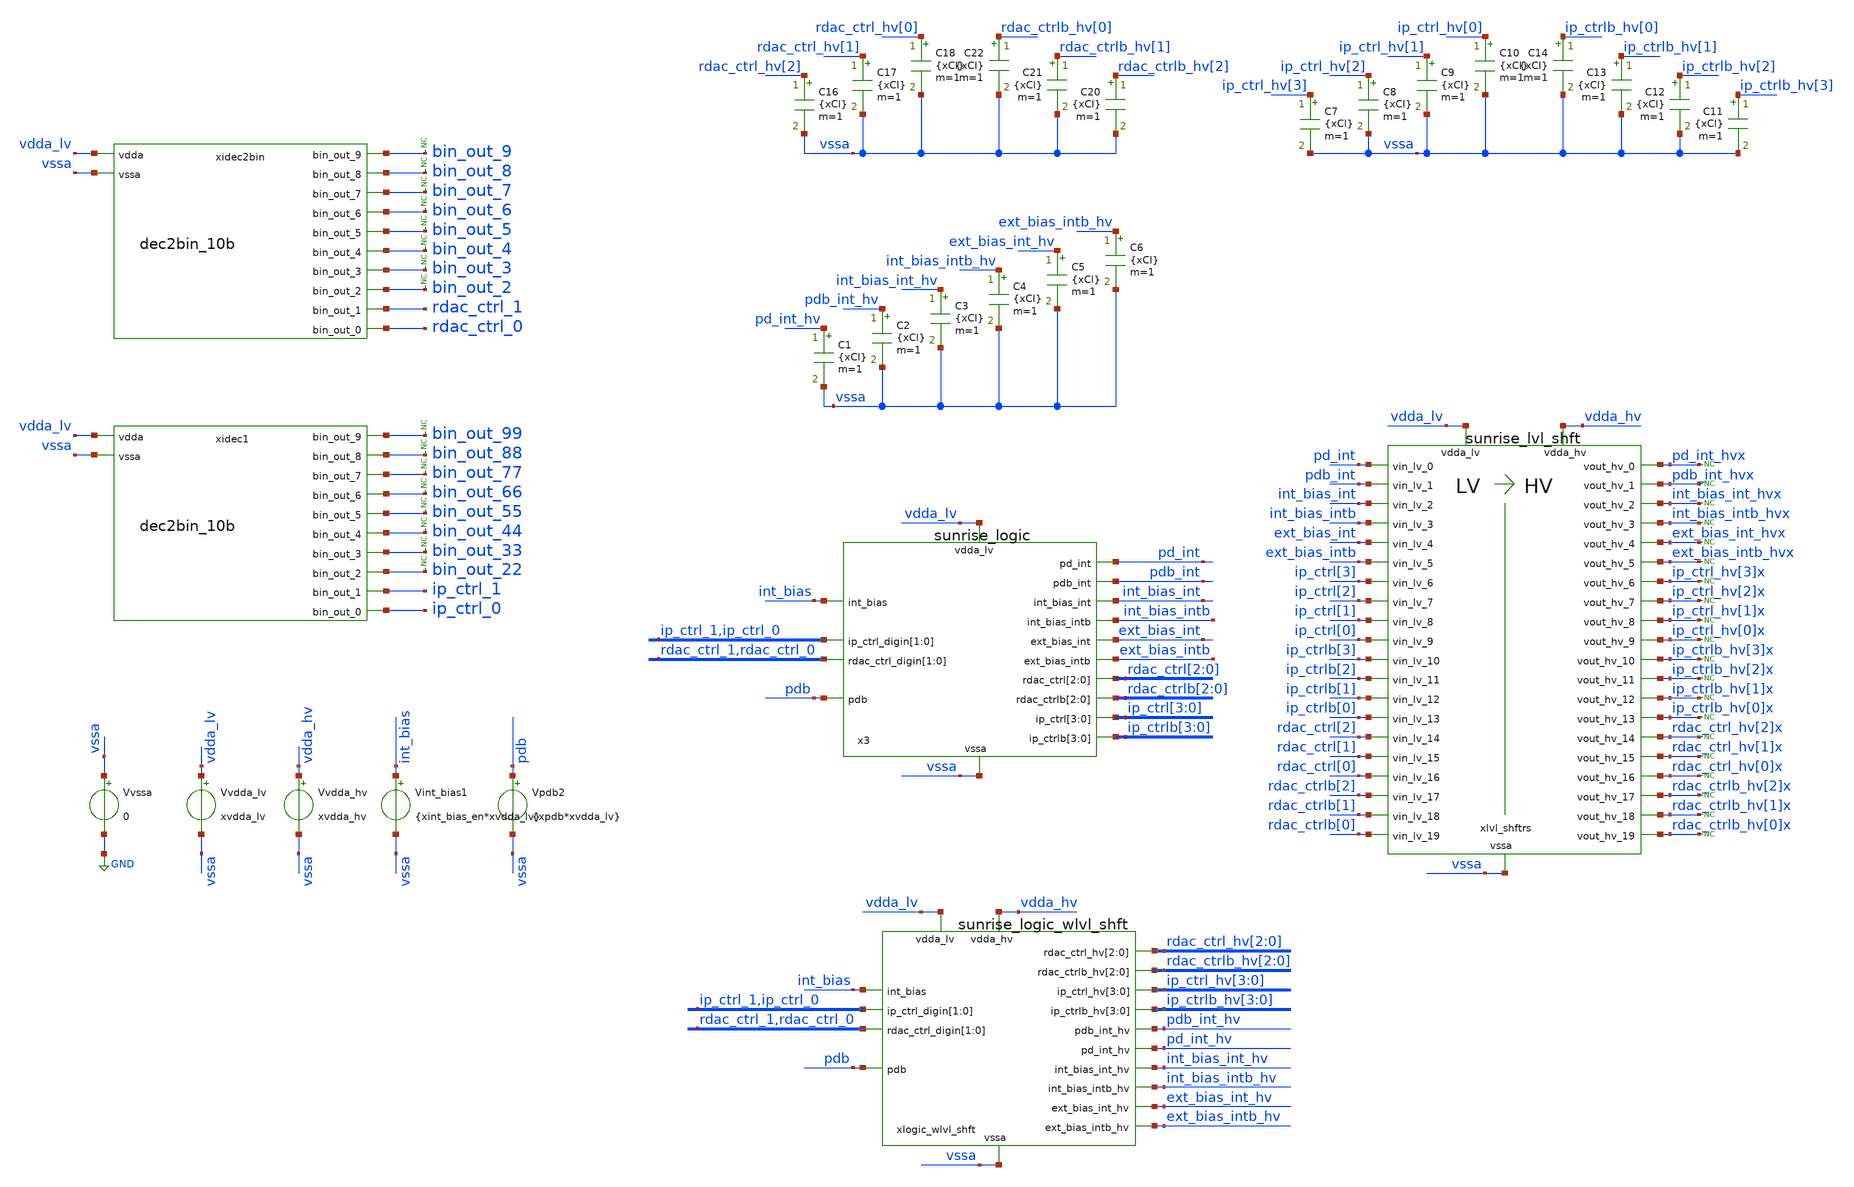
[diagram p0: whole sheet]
** sch_path: Design_Review_3/LVL_SHFT/tb_sunrise_logic.sch
**.subckt tb_sunrise_logic
xidec2bin bin_out_9 bin_out_8 bin_out_7 bin_out_6 bin_out_5 bin_out_4 bin_out_3 bin_out_2
+ rdac_ctrl_1 rdac_ctrl_0 vdda_lv vssa dec2bin_10b dec_code=dec_code_var
* noconn bin_out_9
* noconn bin_out_8
* noconn bin_out_7
* noconn bin_out_6
* noconn bin_out_5
* noconn bin_out_4
* noconn bin_out_3
* noconn bin_out_2
xidec1 bin_out_99 bin_out_88 bin_out_77 bin_out_66 bin_out_55 bin_out_44 bin_out_33 bin_out_22
+ ip_ctrl_1 ip_ctrl_0 vdda_lv vssa dec2bin_10b dec_code=dec_code_var
* noconn bin_out_99
* noconn bin_out_88
* noconn bin_out_77
* noconn bin_out_66
* noconn bin_out_55
* noconn bin_out_44
* noconn bin_out_33
* noconn bin_out_22
Vvssa vssa GND 0
Vvdda_hv vdda_hv vssa xvdda_hv
Vvdda_lv vdda_lv vssa xvdda_lv
C2 pdb_int_hv vssa {xCl} m=1
C3 int_bias_int_hv vssa {xCl} m=1
C4 int_bias_intb_hv vssa {xCl} m=1
C5 ext_bias_int_hv vssa {xCl} m=1
C6 ext_bias_intb_hv vssa {xCl} m=1
C7 ip_ctrl_hv[3] vssa {xCl} m=1
C8 ip_ctrl_hv[2] vssa {xCl} m=1
C9 ip_ctrl_hv[1] vssa {xCl} m=1
C10 ip_ctrl_hv[0] vssa {xCl} m=1
C11 ip_ctrlb_hv[3] vssa {xCl} m=1
C12 ip_ctrlb_hv[2] vssa {xCl} m=1
C13 ip_ctrlb_hv[1] vssa {xCl} m=1
C14 ip_ctrlb_hv[0] vssa {xCl} m=1
C16 rdac_ctrl_hv[2] vssa {xCl} m=1
C17 rdac_ctrl_hv[1] vssa {xCl} m=1
C18 rdac_ctrl_hv[0] vssa {xCl} m=1
C20 rdac_ctrlb_hv[2] vssa {xCl} m=1
C21 rdac_ctrlb_hv[1] vssa {xCl} m=1
C22 rdac_ctrlb_hv[0] vssa {xCl} m=1
xlvl_shftrs vdda_hv vdda_lv pd_int pd_int_hvx vssa pdb_int_hvx pdb_int int_bias_int_hvx int_bias_int
+ int_bias_intb int_bias_intb_hvx ext_bias_int_hvx ext_bias_int ext_bias_intb ext_bias_intb_hvx ip_ctrl_hv[3]x
+ ip_ctrl[3] ip_ctrl_hv[2]x ip_ctrl[2] ip_ctrl[1] ip_ctrl_hv[1]x ip_ctrl_hv[0]x ip_ctrl[0] ip_ctrlb_hv[3]x
+ ip_ctrlb[3] ip_ctrlb_hv[2]x ip_ctrlb[2] ip_ctrlb[1] ip_ctrlb_hv[1]x ip_ctrlb_hv[0]x ip_ctrlb[0]
+ rdac_ctrl_hv[2]x rdac_ctrl[2] rdac_ctrl_hv[1]x rdac_ctrl[1] rdac_ctrl[0] rdac_ctrl_hv[0]x rdac_ctrlb_hv[2]x
+ rdac_ctrlb[2] rdac_ctrlb[1] rdac_ctrlb_hv[1]x rdac_ctrlb_hv[0]x rdac_ctrlb[0] sunrise_lvl_shft
C1 pd_int_hv vssa {xCl} m=1
x3 vdda_lv pd_int pdb_int int_bias_int int_bias_intb int_bias pdb ext_bias_int ext_bias_intb
+ rdac_ctrl_1 rdac_ctrl_0 rdac_ctrl[2] rdac_ctrl[1] rdac_ctrl[0] ip_ctrl[3] ip_ctrl[2] ip_ctrl[1] ip_ctrl[0]
+ ip_ctrl_1 ip_ctrl_0 rdac_ctrlb[2] rdac_ctrlb[1] rdac_ctrlb[0] ip_ctrlb[3] ip_ctrlb[2] ip_ctrlb[1] ip_ctrlb[0]
+ vssa sunrise_logic
Vint_bias1 int_bias vssa {xint_bias_en*xvdda_lv}
Vpdb2 pdb vssa {xpdb*xvdda_lv}
xlogic_wlvl_shft vdda_hv vdda_lv rdac_ctrl_hv[2] rdac_ctrl_hv[1] rdac_ctrl_hv[0] rdac_ctrlb_hv[2]
+ rdac_ctrlb_hv[1] rdac_ctrlb_hv[0] ip_ctrl_hv[3] ip_ctrl_hv[2] ip_ctrl_hv[1] ip_ctrl_hv[0] ip_ctrlb_hv[3]
+ ip_ctrlb_hv[2] ip_ctrlb_hv[1] ip_ctrlb_hv[0] int_bias ip_ctrl_1 ip_ctrl_0 rdac_ctrl_1 rdac_ctrl_0 pdb pdb_int_hv
+ pd_int_hv int_bias_int_hv int_bias_intb_hv ext_bias_int_hv ext_bias_intb_hv vssa sunrise_logic_wlvl_shft
* noconn pd_int_hvx
* noconn pdb_int_hvx
* noconn int_bias_int_hvx
* noconn int_bias_intb_hvx
* noconn ext_bias_int_hvx
* noconn ext_bias_intb_hvx
* noconn ip_ctrl_hv[3]x
* noconn ip_ctrl_hv[2]x
* noconn ip_ctrl_hv[1]x
* noconn ip_ctrl_hv[0]x
* noconn ip_ctrlb_hv[3]x
* noconn ip_ctrlb_hv[2]x
* noconn ip_ctrlb_hv[1]x
* noconn ip_ctrlb_hv[0]x
* noconn rdac_ctrl_hv[2]x
* noconn rdac_ctrl_hv[1]x
* noconn rdac_ctrl_hv[0]x
* noconn rdac_ctrlb_hv[2]x
* noconn rdac_ctrlb_hv[1]x
* noconn rdac_ctrlb_hv[0]x
**** begin user architecture code

** opencircuitdesign pdks install
.lib /home/slice/pdk/iHP/IHP-Open-PDK/ihp-sg13g2/libs.tech/ngspice/models/cornerMOSlv.lib mos_tt
.lib /home/slice/pdk/iHP/IHP-Open-PDK/ihp-sg13g2/libs.tech/ngspice/models/cornerMOShv.lib mos_tt
.lib /home/slice/pdk/iHP/IHP-Open-PDK/ihp-sg13g2/libs.tech/ngspice/models/cornerRES.lib res_typ
* SG13G2 STD CELLS
*.include /home/slice/pdk/iHP/IHP-Open-PDK/ihp-sg13g2/libs.ref/sg13g2_stdcell/spice/sg13g2_stdcell.spice
* SG13CMOS5L STD CELLS
.include /home/slice/pdk/iHP/IHP-Open-PDK/ihp-sg13cmos5l/libs.ref/sg13cmos5l_stdcell/spice/sg13cmos5l_stdcell.spice

*.lib /home/slice/pdk/iHP/IHP-Open-PDK/ihp-sg13g2/libs.tech/ngspice/models/cornerMOShv.lib mos_ss
*.lib /home/slice/pdk/iHP/IHP-Open-PDK/ihp-sg13g2/libs.tech/ngspice/models/cornerRES.lib res_wcs


** PARAMETERS **

* global parameters
.param xvdda_hv = 3.3
.csparam xvdda_hv_var = 'xvdda_hv'
.param xvdda_lv = 1.5
.csparam xvdda_lv_var = 'xvdda_lv'
.param cor_id = 0
.csparam cor_id_var = 'cor_id'
.param xtsim = 2u
.csparam xtsim_var = 'xtsim'
.param xtstep = 1n
.csparam xtstep_var = 'xtstep'
.param xint_bias_en = 1
* active lo => 0 = pd
.param xpdb = 0
.param xtrf = 20p
.param xCl = 0.1p
.param xstep_en = 1
.param dec_code_var = 3

.temp 27

* vlogA instantiations
.model dec2bin_10b dec2bin_10b

.include tb_sunrise_logic.save

.save all

.control

pre_osdi dec2bin_10b.osdi

set xTj = ( 27 )
let xTj_var  = $xTj
set temp = $xTj

** 1. TRAN ANALYSIS **

  tran $&xtstep_var $&xtsim_var
  *** always put remzerovec after the analysis!!!
  remzerovec
  write tb_sunrise_logic_tran.raw

  setplot
*quit 0
.endc




**** end user architecture code
**.ends
.GLOBAL GND
.end
